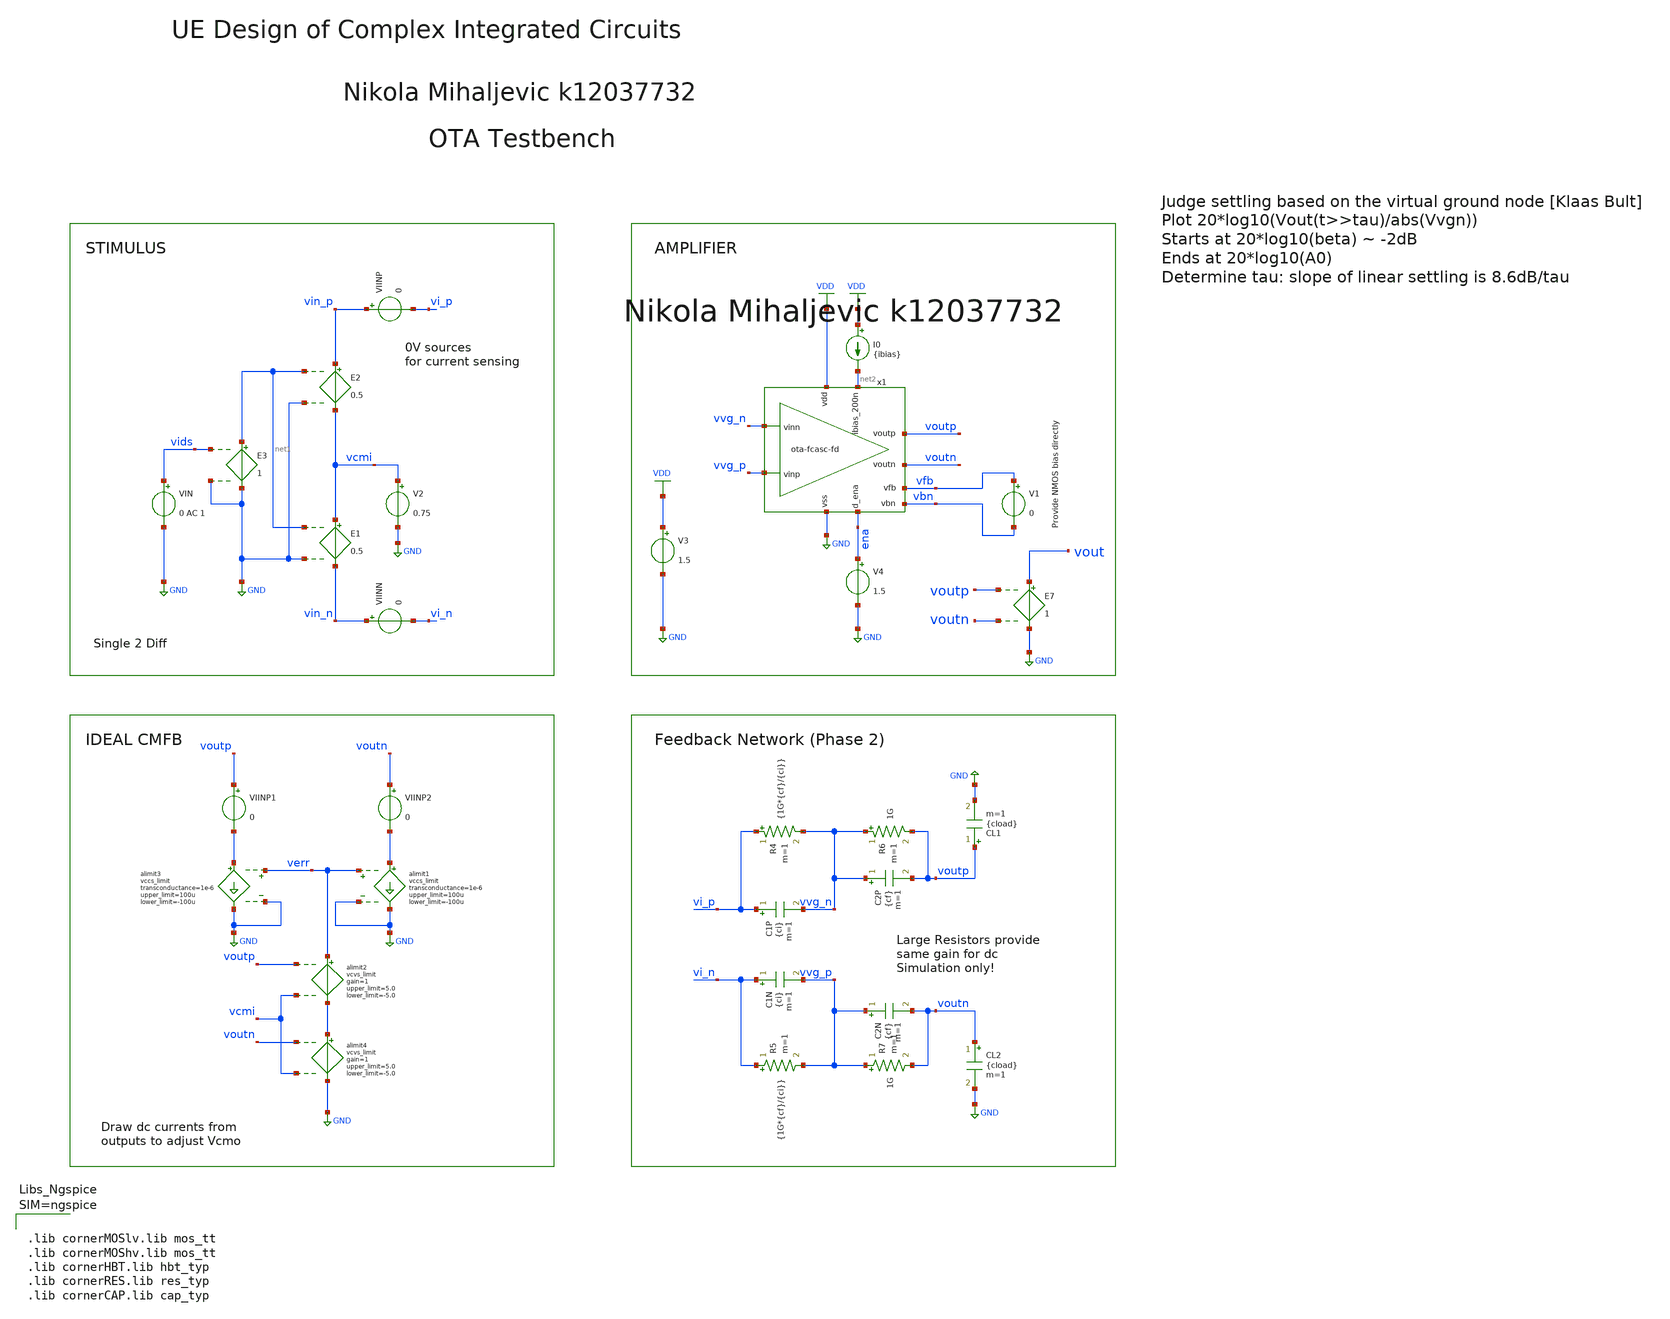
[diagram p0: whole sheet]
** sch_path: ota-fcasc-fd_tb-cl.sch
**.subckt ota-fcasc-fd_tb-cl
V3 VDD GND 1.5
V2 vcmi GND 0.75
E1 vcmi vin_n net1 GND 0.5
E2 vin_p vcmi net1 GND 0.5
VIN vids GND 0 AC 1
E3 net1 GND vids GND 1
VIINP vin_p vi_p 0
VIINN vin_n vi_n 0
V4 ena GND 1.5
E7 vout GND voutp voutn 1
CL2 voutn GND {cload} m=1
CL1 voutp GND {cload} m=1
I0 VDD net2 {ibias}
C2P vvg_n voutp {cf} m=1
C2N vvg_p voutn {cf} m=1
C1P vi_p vvg_n {ci} m=1
C1N vi_n vvg_p {ci} m=1
R4 vi_p vvg_n {1G*{cf}/{ci}} m=1
R5 vi_n vvg_p {1G*{cf}/{ci}} m=1
R6 vvg_n voutp 1G m=1
R7 vvg_p voutn 1G m=1
V1 vfb vbn 0
x1 VDD vfb voutp voutn vvg_p vvg_n net2 ena GND vbn ota-fcasc-fd
**** begin user architecture code


.include ota-fcasc-fd_tb-cl.save
.options savecurrents sparse
.temp 27
.param ibias=0.2u
.param ci=500f
.param fanout=1
.param cload=fanout*ci
.param cf=1.125p

.save all
.control
option numdgt = 3
set doAmpSim = 1

let fb = 128
let osr = 512
let fs = 2*fb*osr
let c1 = 500e-15
let tsettle = 1/fs/2
let vrefp = 1.5
let vrefn = 0
let tau = 119n
let t1 = 1.6u
let t2 = t1+tau


if $doAmpSim eq 1
	setplot const

	let f_min_noise = 1
	let f_max_noise = 1G

	let Acl = 0.444
	let v_step_i = (vrefp-vrefn)
	let v_step_o = -Acl*v_step_i

	let t_rf = 0.0001/fs
	let t_step = 0
	let t_delay = 0
	let t_per = 0

	let tstep = 0.001/fs
	let tstop = 1/fs/2+t_delay
	let tstart = t_delay

	alter @VIN[DC] = 0.0
	alter @VIN[PULSE] = [ 0 $&v_step_i $&t_delay $&t_rf $&t_rf $&t_step $&t_per 0 ]

	noise v(vout) vin dec 100 $&const.f_min_noise $&const.f_max_noise
	tran $&tstep $&tstop $&tstart

	setplot noise1
	plot onoise_spectrum ylog xlog ylabel 'Output Noise'

	setplot tran2
	let vo = v(vout)
	let vcmo = (v(voutp)+v(voutn))/2
	let vvg = v(vvg_p)-v(vvg_n)
	let settle = 20*log10(abs(const.v_step_o)/(abs(vvg)+1u))
	meas tran settle_acc find settle when time=const.tsettle
	meas tran settle_acc_t1 find settle when time=const.t1
	let settle_acc_p8db6 = settle_acc_t1+8.6
	meas tran t_8db6 find time when settle=settle_acc_p8db6
	let t_beta = const.tstart+const.tstep
	meas tran beta_db find settle when time=t_beta

	let tau_meas = t_8db6 - const.t1
	print tau_meas

	let beta_meas = 10^(beta_db/20)
	print beta_meas

	let dcgain_meas_db = settle_acc
	print dcgain_meas_db


	let vod = v(voutp) - v(voutn)
	let e_d_vec = abs(vod-const.v_step_o)

	meas tran err_d find e_d_vec when time=const.t2
	write ota-fcasc-fd_tb-cl.raw
end

reset
op
remzerovec
set appendwrite
write ota-fcasc-fd_tb-cl.raw
.endc




.lib cornerMOSlv.lib mos_tt
.lib cornerMOShv.lib mos_tt
.lib cornerHBT.lib hbt_typ
.lib cornerRES.lib res_typ
.lib cornerCAP.lib cap_typ



**** end user architecture code
**.ends

* expanding   symbol:  /foss/designs/lab1_homework/xschem/ota-fcasc-fd.sym # of pins=10
** sym_path: ota-fcasc-fd.sym
** sch_path: ota-fcasc-fd.sch
.subckt ota-fcasc-fd vdd vfb voutp voutn vinp vinn ibias_200n d_ena vss vbn
*.ipin ibias_200n
*.iopin vdd
*.iopin vss
*.ipin vinp
*.ipin vinn
*.opin voutn
*.ipin d_ena
*.opin voutp
*.ipin vfb
*.opin vbn
XMN5 vbn vbn vss vss sg13_lv_nmos w=1.0u l=5.0u ng=1 m=1 mm_ok=1
XMNSW4 vbn ena_n vss vss sg13_lv_nmos w=1.0u l=5.0u ng=1 m=1 mm_ok=1
XMPSW1 vbp ena vdd vdd sg13_lv_pmos w=1.0u l=5.0u ng=1 m=1 mm_ok=1
XMNEN8 ena ena_n vss vss sg13_lv_nmos w=0.5u l=0.13u ng=1 m=1 mm_ok=1
XMPEN5 ena ena_n vdd vdd sg13_lv_pmos w=1.5u l=0.13u ng=1 m=1 mm_ok=1
XMNSW5 ibias_200n ena vcn vss sg13_lv_nmos w=1.0u l=5.0u ng=1 m=1 mm_ok=1
XMNEN7 ena_n d_ena vss vss sg13_lv_nmos w=0.5u l=0.13u ng=1 m=1 mm_ok=1
XMPEN4 ena_n d_ena vdd vdd sg13_lv_pmos w=1.5u l=0.13u ng=1 m=1 mm_ok=1
XMP1 vd2 vinp vtail vtail sg13_lv_pmos w=10u l=3.5u ng=1 m=1 mm_ok=1
XMP2 vd1 vinn vtail vtail sg13_lv_pmos w=10u l=3.5u ng=1 m=1 mm_ok=1
XMP3 vtail vbp vdd vdd sg13_lv_pmos w=16u l=5.0u ng=2 m=1 mm_ok=1
XMP6 voutp vcp vd4 vdd sg13_lv_pmos w=22.0u l=5.0u ng=4 m=1 mm_ok=1
XMP7 voutn vcp vd5 vdd sg13_lv_pmos w=22.0u l=5.0u ng=4 m=1 mm_ok=1
XMP4 vd4 vbp vdd vdd sg13_lv_pmos w=8.0u l=5.0u ng=1 m=1 mm_ok=1
XMP5 vd5 vbp vdd vdd sg13_lv_pmos w=8.0u l=5.0u ng=1 m=1 mm_ok=1
XMN3 voutp vcn vd1 vss sg13_lv_nmos w=6.5u l=5.0u ng=1 m=1 mm_ok=1
XMN4 voutn vcn vd2 vss sg13_lv_nmos w=6.5u l=5.0u ng=1 m=1 mm_ok=1
XMN1 vd1 vfb vss vss sg13_lv_nmos w=4u l=5.0u ng=1 m=1 mm_ok=1
XMN2 vd2 vfb vss vss sg13_lv_nmos w=4u l=5.0u ng=1 m=1 mm_ok=1
XMPSW2 vcp ena vdd vdd sg13_lv_pmos w=1.0u l=5.0u ng=1 m=1 mm_ok=1
XMNSW1 vfb ena_n vss vss sg13_lv_nmos w=1.0u l=5.0u ng=1 m=1 mm_ok=1
XMNSW2 vcn ena_n vss vss sg13_lv_nmos w=1.0u l=5.0u ng=1 m=1 mm_ok=1
XMN6 ibias_200n vcn vbn vss sg13_lv_nmos w=3.0u l=5.0u ng=1 m=1 mm_ok=1
XMN7 net1 vbn vss vss sg13_lv_nmos w=1.0u l=5.0u ng=1 m=1 mm_ok=1
XMN8 ena_n vcn net1 vss sg13_lv_nmos w=3.0u l=5.0u ng=1 m=1 mm_ok=1
XMP8 vbp vbp vdd vdd sg13_lv_pmos w=4.0u l=5.0u ng=4 m=1 mm_ok=1
XMP9 ena_n vcp vbp vdd sg13_lv_pmos w=11.0u l=5.0u ng=2 m=1 mm_ok=1
XMPSW3 vbp ena vdd vdd sg13_lv_pmos w=1.0u l=5.0u ng=1 m=1 mm_ok=1
XMPSW5 ena_n ena_n vcp vdd sg13_lv_pmos w=1.0u l=5.0u ng=1 m=1 mm_ok=1
XMNSW3 vcn ena_n vss vss sg13_lv_nmos w=1.0u l=5.0u ng=1 m=1 mm_ok=1
XMPSW4 vcp ena vdd vdd sg13_lv_pmos w=1.0u l=5.0u ng=1 m=1 mm_ok=1
.ends

.GLOBAL GND
.GLOBAL VDD
.end
